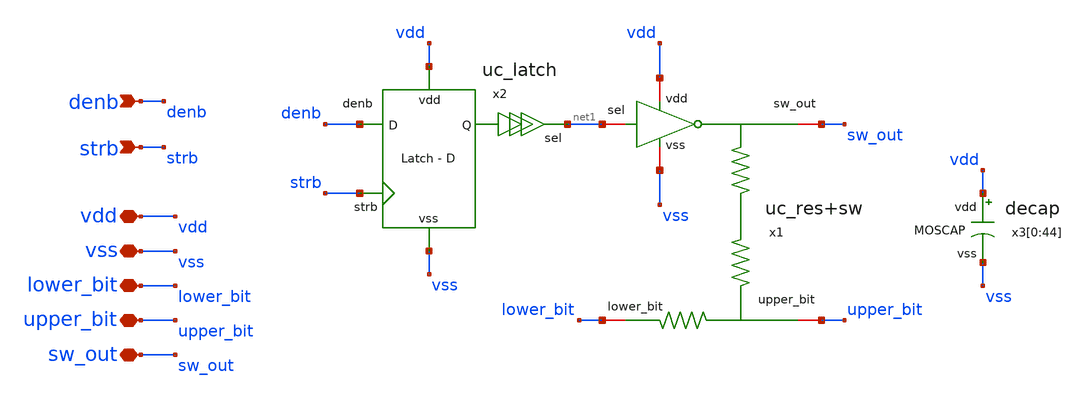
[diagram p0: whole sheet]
** sch_path: xschem/uc_bit_cell/uc_bit_cell.sch
**.subckt uc_bit_cell denb strb vdd vss lower_bit upper_bit sw_out
*.ipin denb
*.ipin strb
*.iopin vdd
*.iopin vss
*.iopin lower_bit
*.iopin upper_bit
*.iopin sw_out
x1 vdd vss net1 lower_bit upper_bit sw_out uc_res+sw
x2 vdd vss strb denb net1 uc_latch
x3[0] vdd vss decap
x3[1] vdd vss decap
x3[2] vdd vss decap
x3[3] vdd vss decap
x3[4] vdd vss decap
x3[5] vdd vss decap
x3[6] vdd vss decap
x3[7] vdd vss decap
x3[8] vdd vss decap
x3[9] vdd vss decap
x3[10] vdd vss decap
x3[11] vdd vss decap
x3[12] vdd vss decap
x3[13] vdd vss decap
x3[14] vdd vss decap
x3[15] vdd vss decap
x3[16] vdd vss decap
x3[17] vdd vss decap
x3[18] vdd vss decap
x3[19] vdd vss decap
x3[20] vdd vss decap
x3[21] vdd vss decap
x3[22] vdd vss decap
x3[23] vdd vss decap
x3[24] vdd vss decap
x3[25] vdd vss decap
x3[26] vdd vss decap
x3[27] vdd vss decap
x3[28] vdd vss decap
x3[29] vdd vss decap
x3[30] vdd vss decap
x3[31] vdd vss decap
x3[32] vdd vss decap
x3[33] vdd vss decap
x3[34] vdd vss decap
x3[35] vdd vss decap
x3[36] vdd vss decap
x3[37] vdd vss decap
x3[38] vdd vss decap
x3[39] vdd vss decap
x3[40] vdd vss decap
x3[41] vdd vss decap
x3[42] vdd vss decap
x3[43] vdd vss decap
x3[44] vdd vss decap
**.ends
.end
